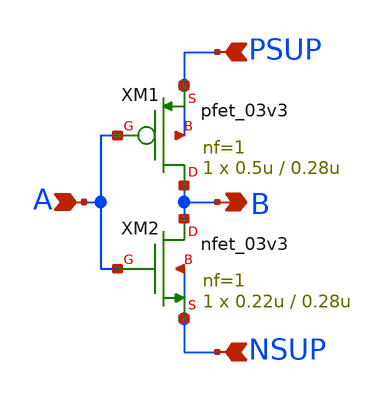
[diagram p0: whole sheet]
** sch_path: xschem/blocks/not/not.sch
**.subckt not PSUP NSUP A B
*.ipin PSUP
*.ipin NSUP
*.ipin A
*.opin B
XM2 B A NSUP NSUP nfet_03v3 L=0.28u W=0.22u nf=1 ad='int((nf+1)/2) * W/nf * 0.18u' as='int((nf+2)/2) * W/nf * 0.18u'
+ pd='2*int((nf+1)/2) * (W/nf + 0.18u)' ps='2*int((nf+2)/2) * (W/nf + 0.18u)' nrd='0.18u / W' nrs='0.18u / W'
+ sa=0 sb=0 sd=0 m=1
XM1 B A PSUP PSUP pfet_03v3 L=0.28u W=0.5u nf=1 ad='int((nf+1)/2) * W/nf * 0.18u' as='int((nf+2)/2) * W/nf * 0.18u'
+ pd='2*int((nf+1)/2) * (W/nf + 0.18u)' ps='2*int((nf+2)/2) * (W/nf + 0.18u)' nrd='0.18u / W' nrs='0.18u / W'
+ sa=0 sb=0 sd=0 m=1
**.ends
.end
